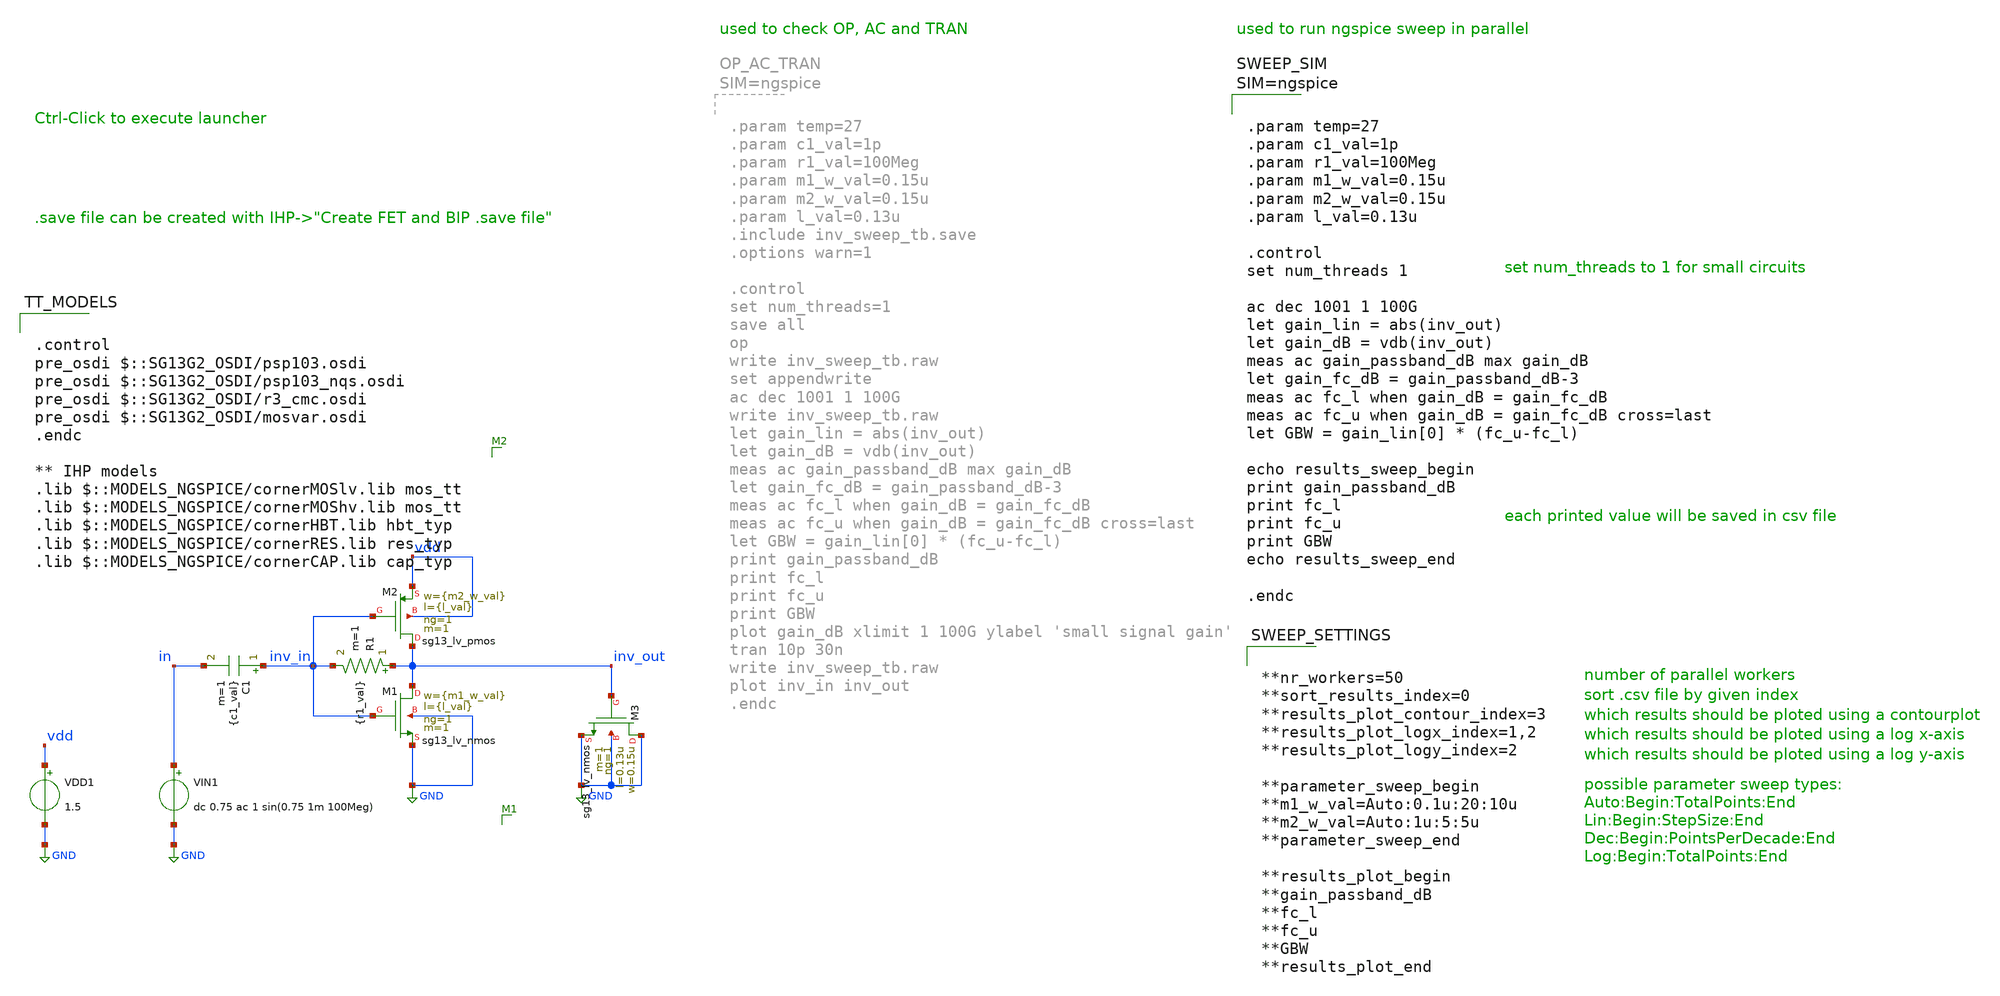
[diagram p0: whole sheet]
** sch_path: ihp-sg13g2/xschem_libs/sg13g2_tests/inv_sweep_tb/schematic/inv_sweep_tb.sch
**.subckt inv_sweep_tb
VDD1 vdd GND 1.5
XM1 inv_out inv_in GND GND sg13_lv_nmos w={m1_w_val} l={l_val} ng=1 m=1 mm_ok=1
XM2 inv_out inv_in vdd vdd sg13_lv_pmos w={m2_w_val} l={l_val} ng=1 m=1 mm_ok=1
XM3 GND inv_out GND GND sg13_lv_nmos w=0.15u l=0.13u ng=1 m=1 mm_ok=1
VIN1 in GND dc 0.75 ac 1 sin(0.75 1m 100Meg)
R1 inv_out inv_in {r1_val} m=1
C1 inv_in in {c1_val} m=1
**** begin user architecture code

.control
pre_osdi $::SG13G2_OSDI/psp103.osdi
pre_osdi $::SG13G2_OSDI/psp103_nqs.osdi
pre_osdi $::SG13G2_OSDI/r3_cmc.osdi
pre_osdi $::SG13G2_OSDI/mosvar.osdi
.endc

** IHP models
.lib $::MODELS_NGSPICE/cornerMOSlv.lib mos_tt
.lib $::MODELS_NGSPICE/cornerMOShv.lib mos_tt
.lib $::MODELS_NGSPICE/cornerHBT.lib hbt_typ
.lib $::MODELS_NGSPICE/cornerRES.lib res_typ
.lib $::MODELS_NGSPICE/cornerCAP.lib cap_typ




.param temp=27
.param c1_val=1p
.param r1_val=100Meg
.param m1_w_val=0.15u
.param m2_w_val=0.15u
.param l_val=0.13u

.control
set num_threads 1

ac dec 1001 1 100G
let gain_lin = abs(inv_out)
let gain_dB = vdb(inv_out)
meas ac gain_passband_dB max gain_dB
let gain_fc_dB = gain_passband_dB-3
meas ac fc_l when gain_dB = gain_fc_dB
meas ac fc_u when gain_dB = gain_fc_dB cross=last
let GBW = gain_lin[0] * (fc_u-fc_l)

echo results_sweep_begin
print gain_passband_dB
print fc_l
print fc_u
print GBW
echo results_sweep_end

.endc





**nr_workers=50
**sort_results_index=0
**results_plot_contour_index=3
**results_plot_logx_index=1,2
**results_plot_logy_index=2

**parameter_sweep_begin
**m1_w_val=Auto:0.1u:20:10u
**m2_w_val=Auto:1u:5:5u
**parameter_sweep_end

**results_plot_begin
**gain_passband_dB
**fc_l
**fc_u
**GBW
**results_plot_end


**** end user architecture code
**.ends
.GLOBAL GND
.end
